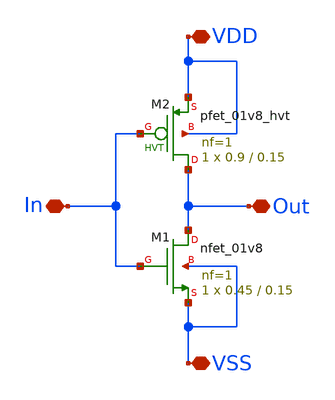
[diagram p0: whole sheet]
** sch_path: HVT/inverter/inverter.sch
**.subckt inverter VDD Out VSS In
*.iopin VDD
*.iopin Out
*.iopin VSS
*.iopin In
XM2 Out In VDD VDD sky130_fd_pr__pfet_01v8_hvt L=0.15 W=0.9 nf=1 ad='int((nf+1)/2) * W/nf * 0.29' as='int((nf+2)/2) * W/nf * 0.29'
+ pd='2*int((nf+1)/2) * (W/nf + 0.29)' ps='2*int((nf+2)/2) * (W/nf + 0.29)' nrd='0.29 / W' nrs='0.29 / W'
+ sa=0 sb=0 sd=0 mult=1 m=1
XM1 Out In VSS VSS sky130_fd_pr__nfet_01v8 L=0.15 W=0.45 nf=1 ad='int((nf+1)/2) * W/nf * 0.29' as='int((nf+2)/2) * W/nf * 0.29'
+ pd='2*int((nf+1)/2) * (W/nf + 0.29)' ps='2*int((nf+2)/2) * (W/nf + 0.29)' nrd='0.29 / W' nrs='0.29 / W'
+ sa=0 sb=0 sd=0 mult=1 m=1
**.ends
.end
